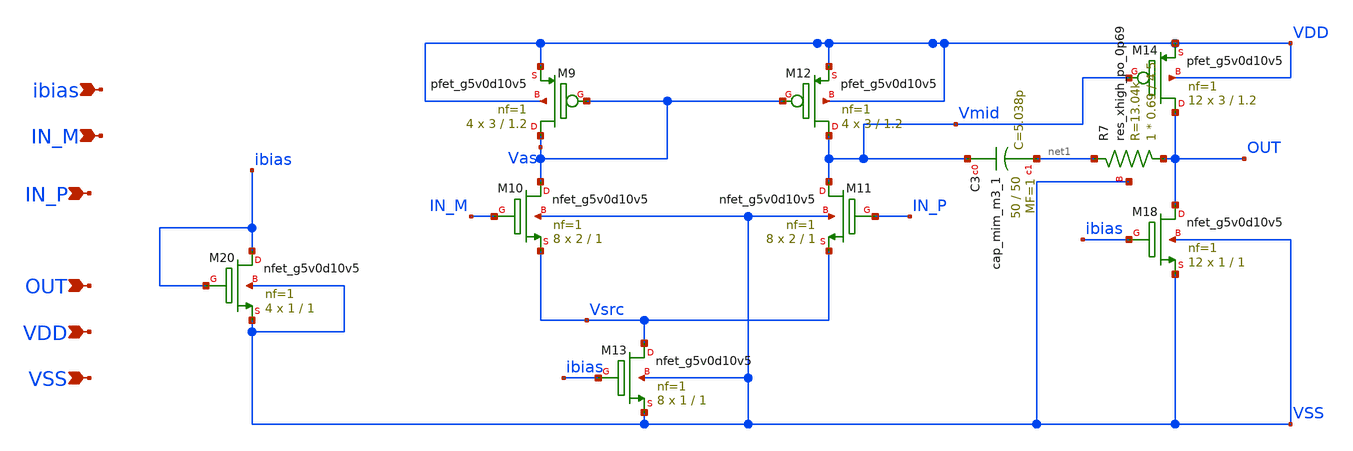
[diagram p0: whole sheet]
** sch_path: ldo_new_bg_DA_20230921/OTA_erroramp_jm.sch
**.subckt OTA_erroramp_jm IN_M IN_P OUT VDD VSS ibias
*.ipin IN_M
*.ipin IN_P
*.ipin OUT
*.ipin VDD
*.ipin VSS
*.ipin ibias
XM9 Vas Vas VDD VDD sky130_fd_pr__pfet_g5v0d10v5 L=1.2 W=3 nf=1 ad='int((nf+1)/2) * W/nf * 0.29' as='int((nf+2)/2) * W/nf * 0.29'
+ pd='2*int((nf+1)/2) * (W/nf + 0.29)' ps='2*int((nf+2)/2) * (W/nf + 0.29)' nrd='0.29 / W' nrs='0.29 / W'
+ sa=0 sb=0 sd=0 mult=4 m=4
XM10 Vas IN_M Vsrc VSS sky130_fd_pr__nfet_g5v0d10v5 L=1 W=2 nf=1 ad='int((nf+1)/2) * W/nf * 0.29' as='int((nf+2)/2) * W/nf * 0.29'
+ pd='2*int((nf+1)/2) * (W/nf + 0.29)' ps='2*int((nf+2)/2) * (W/nf + 0.29)' nrd='0.29 / W' nrs='0.29 / W'
+ sa=0 sb=0 sd=0 mult=8 m=8
XM11 Vmid IN_P Vsrc VSS sky130_fd_pr__nfet_g5v0d10v5 L=1 W=2 nf=1 ad='int((nf+1)/2) * W/nf * 0.29' as='int((nf+2)/2) * W/nf * 0.29'
+ pd='2*int((nf+1)/2) * (W/nf + 0.29)' ps='2*int((nf+2)/2) * (W/nf + 0.29)' nrd='0.29 / W' nrs='0.29 / W'
+ sa=0 sb=0 sd=0 mult=8 m=8
XM12 Vmid Vas VDD VDD sky130_fd_pr__pfet_g5v0d10v5 L=1.2 W=3 nf=1 ad='int((nf+1)/2) * W/nf * 0.29' as='int((nf+2)/2) * W/nf * 0.29'
+ pd='2*int((nf+1)/2) * (W/nf + 0.29)' ps='2*int((nf+2)/2) * (W/nf + 0.29)' nrd='0.29 / W' nrs='0.29 / W'
+ sa=0 sb=0 sd=0 mult=4 m=4
XM13 Vsrc ibias VSS VSS sky130_fd_pr__nfet_g5v0d10v5 L=1 W=1 nf=1 ad='int((nf+1)/2) * W/nf * 0.29' as='int((nf+2)/2) * W/nf * 0.29'
+ pd='2*int((nf+1)/2) * (W/nf + 0.29)' ps='2*int((nf+2)/2) * (W/nf + 0.29)' nrd='0.29 / W' nrs='0.29 / W'
+ sa=0 sb=0 sd=0 mult=8 m=8
XM14 OUT Vmid VDD VDD sky130_fd_pr__pfet_g5v0d10v5 L=1.2 W=3 nf=1 ad='int((nf+1)/2) * W/nf * 0.29' as='int((nf+2)/2) * W/nf * 0.29'
+ pd='2*int((nf+1)/2) * (W/nf + 0.29)' ps='2*int((nf+2)/2) * (W/nf + 0.29)' nrd='0.29 / W' nrs='0.29 / W'
+ sa=0 sb=0 sd=0 mult=12 m=12
XM18 OUT ibias VSS VSS sky130_fd_pr__nfet_g5v0d10v5 L=1 W=1 nf=1 ad='int((nf+1)/2) * W/nf * 0.29' as='int((nf+2)/2) * W/nf * 0.29'
+ pd='2*int((nf+1)/2) * (W/nf + 0.29)' ps='2*int((nf+2)/2) * (W/nf + 0.29)' nrd='0.29 / W' nrs='0.29 / W'
+ sa=0 sb=0 sd=0 mult=12 m=12
XC3 Vmid net1 sky130_fd_pr__cap_mim_m3_1 W=50 L=50 MF=1 m=1
XR7 OUT net1 VSS sky130_fd_pr__res_xhigh_po_0p69 L=4.5 mult=1 m=1
XM20 ibias ibias VSS VSS sky130_fd_pr__nfet_g5v0d10v5 L=1 W=1 nf=1 ad='int((nf+1)/2) * W/nf * 0.29' as='int((nf+2)/2) * W/nf * 0.29'
+ pd='2*int((nf+1)/2) * (W/nf + 0.29)' ps='2*int((nf+2)/2) * (W/nf + 0.29)' nrd='0.29 / W' nrs='0.29 / W'
+ sa=0 sb=0 sd=0 mult=4 m=4
**.ends
.end
